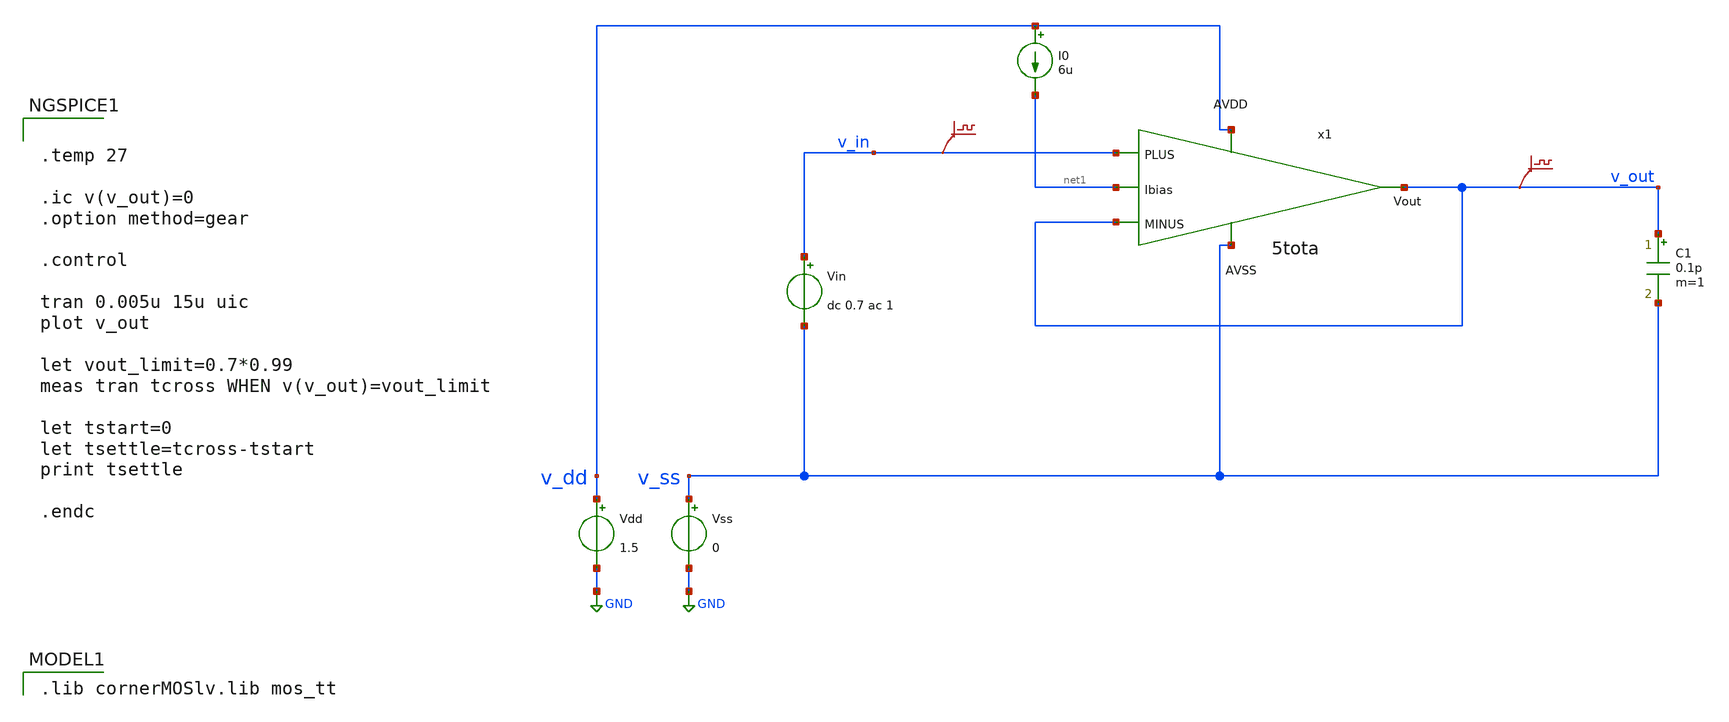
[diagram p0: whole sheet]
** sch_path: Designs/otas/1_schematics/tb_5t_ota_tran.sch
* Designs/otas/1_schematics/5tota.sch:
* (c) 2025 Thesis_HP, Apache-2.0 license
**.subckt tb_5t_ota_tran
Vdd v_dd GND 1.5
Vss v_ss GND 0
C1 v_out v_ss 0.1p m=1
Vin v_in v_ss dc 0.7 ac 1
I0 v_dd net1 6u
.save v(v_in)
.save v(v_out)
x1 v_dd v_out net1 v_in v_out v_ss 5tota
**** begin user architecture code
 .lib cornerMOSlv.lib mos_tt



.temp 27

.ic v(v_out)=0
.option method=gear

.control

tran 0.005u 15u uic
plot v_out

let vout_limit=0.7*0.99
meas tran tcross WHEN v(v_out)=vout_limit

let tstart=0
let tsettle=tcross-tstart
print tsettle

.endc


**** end user architecture code
**.ends

* expanding   symbol:  /foss/designs/thesis_hp/designs/otas/1_schematics/5tota.sym # of pins=6
** sym_path: Designs/otas/1_schematics/5tota.sym
** sch_path: Designs/otas/1_schematics/5tota.sch
.subckt 5tota AVDD Vout Ibias PLUS MINUS AVSS
*.ipin PLUS
*.ipin MINUS
*.opin Vout
*.ipin AVDD
*.ipin AVSS
*.ipin Ibias
XM1 Vout MINUS net2 AVSS sg13_lv_nmos w=2u l=5u ng=1 m=1 mm_ok=1
XM3 net1 PLUS net2 AVSS sg13_lv_nmos w=2u l=5u ng=1 m=1 mm_ok=1
XM5 Vout net1 AVDD AVDD sg13_lv_pmos w=1.5u l=5u ng=1 m=1 mm_ok=1
XM7 net1 net1 AVDD AVDD sg13_lv_pmos w=1.5u l=5u ng=1 m=1 mm_ok=1
XM6 net2 net3 AVSS AVSS sg13_lv_nmos w=0.5u l=5u ng=1 m=1 mm_ok=1
XM4 AVDD AVDD net4 AVSS sg13_lv_nmos w=2.5u l=5u ng=1 m=1 mm_ok=1
XM2 net4 net3 AVSS AVSS sg13_lv_nmos w=2.5u l=5u ng=1 m=1 mm_ok=1
XM9 net3 net3 AVSS AVSS sg13_lv_nmos w=2.5u l=5u ng=1 m=1 mm_ok=1
XM8 Ibias AVDD net3 AVSS sg13_lv_nmos w=2.5u l=5u ng=1 m=1 mm_ok=1
.ends

.GLOBAL GND
.end
